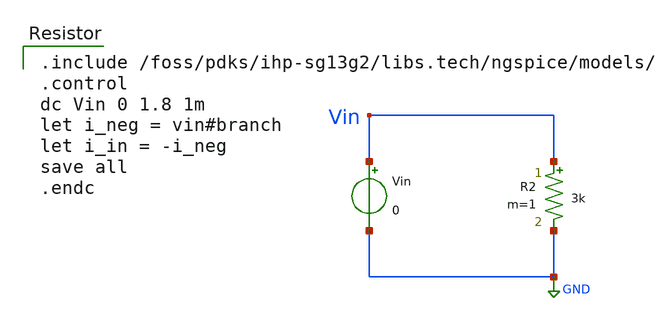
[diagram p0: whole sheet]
** sch_path: content/simulation_files/xschem/01_Resistor_DC_sweep.sch
**.subckt 01_Resistor_DC_sweep
Vin Vin GND 0
R2 Vin GND 3k m=1
**** begin user architecture code

.include /foss/pdks/ihp-sg13g2/libs.tech/ngspice/models/
.control
dc Vin 0 1.8 1m
let i_neg = vin#branch
let i_in = -i_neg
save all
.endc

**** end user architecture code
**.ends
.GLOBAL GND
.end
